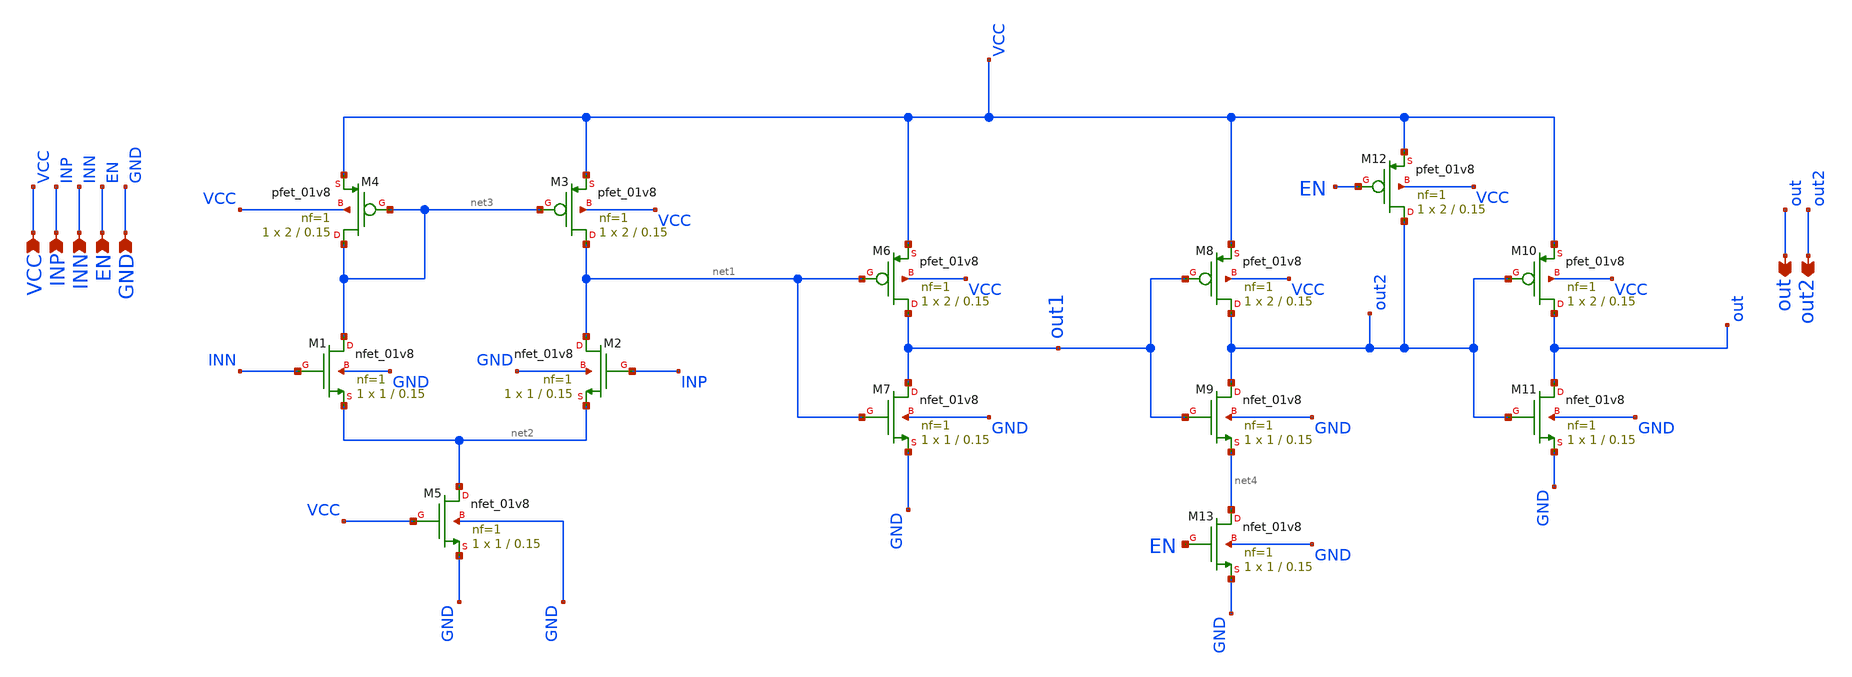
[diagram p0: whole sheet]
** sch_path: Kelompok7_Comparator/xsch/dsrt_comparator.sch
**.subckt dsrt_comparator VCC GND INP INN EN out out2
*.ipin VCC
*.ipin GND
*.ipin INP
*.ipin INN
*.ipin EN
*.opin out
*.opin out2
XM1 net3 INN net2 GND sky130_fd_pr__nfet_01v8 L=0.15 W=1 nf=1 ad='int((1 + 1)/2) * 1 / 1 * 0.29' as='int((1 + 2)/2) * 1 / 1 * 0.29'
+ pd='2*int((1 + 1)/2) * (1 / 1 + 0.29)' ps='2*int((1 + 2)/2) * (1 / 1 + 0.29)' nrd='0.29 / 1 ' nrs='0.29 / 1 '
+ sa=0 sb=0 sd=0 mult=1 m=1
XM2 net1 INP net2 GND sky130_fd_pr__nfet_01v8 L=0.15 W=1 nf=1 ad='int((1 + 1)/2) * 1 / 1 * 0.29' as='int((1 + 2)/2) * 1 / 1 * 0.29'
+ pd='2*int((1 + 1)/2) * (1 / 1 + 0.29)' ps='2*int((1 + 2)/2) * (1 / 1 + 0.29)' nrd='0.29 / 1 ' nrs='0.29 / 1 '
+ sa=0 sb=0 sd=0 mult=1 m=1
XM3 net1 net3 VCC VCC sky130_fd_pr__pfet_01v8 L=0.15 W=2 nf=1 ad='int((1 + 1)/2) * 2 / 1 * 0.29' as='int((1 + 2)/2) * 2 / 1 * 0.29'
+ pd='2*int((1 + 1)/2) * (2 / 1 + 0.29)' ps='2*int((1 + 2)/2) * (2 / 1 + 0.29)' nrd='0.29 / 2 ' nrs='0.29 / 2 '
+ sa=0 sb=0 sd=0 mult=1 m=1
XM4 net3 net3 VCC VCC sky130_fd_pr__pfet_01v8 L=0.15 W=2 nf=1 ad='int((1 + 1)/2) * 2 / 1 * 0.29' as='int((1 + 2)/2) * 2 / 1 * 0.29'
+ pd='2*int((1 + 1)/2) * (2 / 1 + 0.29)' ps='2*int((1 + 2)/2) * (2 / 1 + 0.29)' nrd='0.29 / 2 ' nrs='0.29 / 2 '
+ sa=0 sb=0 sd=0 mult=1 m=1
XM5 net2 VCC GND GND sky130_fd_pr__nfet_01v8 L=0.15 W=1 nf=1 ad='int((1 + 1)/2) * 1 / 1 * 0.29' as='int((1 + 2)/2) * 1 / 1 * 0.29'
+ pd='2*int((1 + 1)/2) * (1 / 1 + 0.29)' ps='2*int((1 + 2)/2) * (1 / 1 + 0.29)' nrd='0.29 / 1 ' nrs='0.29 / 1 '
+ sa=0 sb=0 sd=0 mult=1 m=1
XM6 out1 net1 VCC VCC sky130_fd_pr__pfet_01v8 L=0.15 W=2 nf=1 ad='int((1 + 1)/2) * 2 / 1 * 0.29' as='int((1 + 2)/2) * 2 / 1 * 0.29'
+ pd='2*int((1 + 1)/2) * (2 / 1 + 0.29)' ps='2*int((1 + 2)/2) * (2 / 1 + 0.29)' nrd='0.29 / 2 ' nrs='0.29 / 2 '
+ sa=0 sb=0 sd=0 mult=1 m=1
XM7 out1 net1 GND GND sky130_fd_pr__nfet_01v8 L=0.15 W=1 nf=1 ad='int((1 + 1)/2) * 1 / 1 * 0.29' as='int((1 + 2)/2) * 1 / 1 * 0.29'
+ pd='2*int((1 + 1)/2) * (1 / 1 + 0.29)' ps='2*int((1 + 2)/2) * (1 / 1 + 0.29)' nrd='0.29 / 1 ' nrs='0.29 / 1 '
+ sa=0 sb=0 sd=0 mult=1 m=1
XM8 out2 out1 VCC VCC sky130_fd_pr__pfet_01v8 L=0.15 W=2 nf=1 ad='int((1 + 1)/2) * 2 / 1 * 0.29' as='int((1 + 2)/2) * 2 / 1 * 0.29'
+ pd='2*int((1 + 1)/2) * (2 / 1 + 0.29)' ps='2*int((1 + 2)/2) * (2 / 1 + 0.29)' nrd='0.29 / 2 ' nrs='0.29 / 2 '
+ sa=0 sb=0 sd=0 mult=1 m=1
XM9 out2 out1 net4 GND sky130_fd_pr__nfet_01v8 L=0.15 W=1 nf=1 ad='int((1 + 1)/2) * 1 / 1 * 0.29' as='int((1 + 2)/2) * 1 / 1 * 0.29'
+ pd='2*int((1 + 1)/2) * (1 / 1 + 0.29)' ps='2*int((1 + 2)/2) * (1 / 1 + 0.29)' nrd='0.29 / 1 ' nrs='0.29 / 1 '
+ sa=0 sb=0 sd=0 mult=1 m=1
XM10 out out2 VCC VCC sky130_fd_pr__pfet_01v8 L=0.15 W=2 nf=1 ad='int((1 + 1)/2) * 2 / 1 * 0.29' as='int((1 + 2)/2) * 2 / 1 * 0.29'
+ pd='2*int((1 + 1)/2) * (2 / 1 + 0.29)' ps='2*int((1 + 2)/2) * (2 / 1 + 0.29)' nrd='0.29 / 2 ' nrs='0.29 / 2 '
+ sa=0 sb=0 sd=0 mult=1 m=1
XM11 out out2 GND GND sky130_fd_pr__nfet_01v8 L=0.15 W=1 nf=1 ad='int((1 + 1)/2) * 1 / 1 * 0.29' as='int((1 + 2)/2) * 1 / 1 * 0.29'
+ pd='2*int((1 + 1)/2) * (1 / 1 + 0.29)' ps='2*int((1 + 2)/2) * (1 / 1 + 0.29)' nrd='0.29 / 1 ' nrs='0.29 / 1 '
+ sa=0 sb=0 sd=0 mult=1 m=1
XM13 net4 EN GND GND sky130_fd_pr__nfet_01v8 L=0.15 W=1 nf=1 ad='int((1 + 1)/2) * 1 / 1 * 0.29' as='int((1 + 2)/2) * 1 / 1 * 0.29'
+ pd='2*int((1 + 1)/2) * (1 / 1 + 0.29)' ps='2*int((1 + 2)/2) * (1 / 1 + 0.29)' nrd='0.29 / 1 ' nrs='0.29 / 1 '
+ sa=0 sb=0 sd=0 mult=1 m=1
XM12 out2 EN VCC VCC sky130_fd_pr__pfet_01v8 L=0.15 W=2 nf=1 ad='int((1 + 1)/2) * 2 / 1 * 0.29' as='int((1 + 2)/2) * 2 / 1 * 0.29'
+ pd='2*int((1 + 1)/2) * (2 / 1 + 0.29)' ps='2*int((1 + 2)/2) * (2 / 1 + 0.29)' nrd='0.29 / 2 ' nrs='0.29 / 2 '
+ sa=0 sb=0 sd=0 mult=1 m=1
**** begin user architecture code
 .lib /foss/pdks/sky130A/libs.tech/ngspice/sky130.lib.spice tt

.param mc_mm_switch=0
.param mc_pr_switch=1



.option wnflag=0
.option savecurrents
.control
save all
*dc v2 0 1.8 0.01
*tran 10ps 30ns
tran 10n 100u
*plot inn inp out1 out2 out
plot inn inp out en
op
.endc


**** end user architecture code
**.ends
.end
